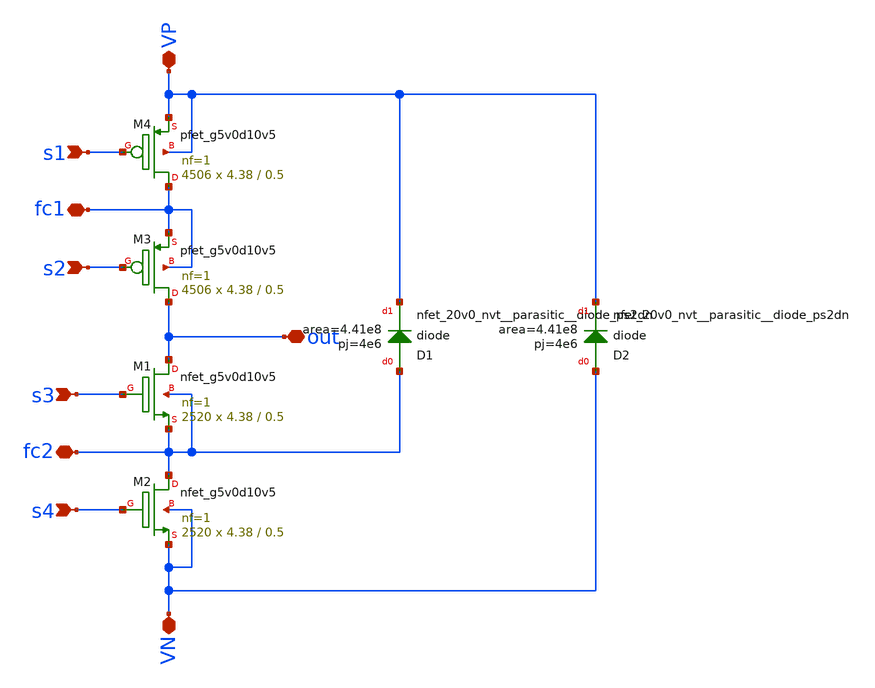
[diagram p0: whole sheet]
** sch_path: xschem/hierarchy_sch/power_stage_diode.sch
**.subckt power_stage_diode VP s1 s2 out s3 s4 VN fc1 fc2
*.iopin VP
*.ipin s1
*.ipin s2
*.iopin out
*.ipin s3
*.ipin s4
*.iopin VN
*.iopin fc1
*.iopin fc2
XM3 out s2 fc1 fc1 sky130_fd_pr__pfet_g5v0d10v5 L=0.5 W=4.38 nf=1 ad='int((nf+1)/2) * W/nf * 0.29' as='int((nf+2)/2) * W/nf * 0.29'
+ pd='2*int((nf+1)/2) * (W/nf + 0.29)' ps='2*int((nf+2)/2) * (W/nf + 0.29)' nrd='0.29 / W' nrs='0.29 / W'
+ sa=0 sb=0 sd=0 mult=4506 m=4506
XM4 fc1 s1 VP VP sky130_fd_pr__pfet_g5v0d10v5 L=0.5 W=4.38 nf=1 ad='int((nf+1)/2) * W/nf * 0.29' as='int((nf+2)/2) * W/nf * 0.29'
+ pd='2*int((nf+1)/2) * (W/nf + 0.29)' ps='2*int((nf+2)/2) * (W/nf + 0.29)' nrd='0.29 / W' nrs='0.29 / W'
+ sa=0 sb=0 sd=0 mult=4506 m=4506
XM1 out s3 fc2 fc2 sky130_fd_pr__nfet_g5v0d10v5 L=0.5 W=4.38 nf=1 ad='int((nf+1)/2) * W/nf * 0.29' as='int((nf+2)/2) * W/nf * 0.29'
+ pd='2*int((nf+1)/2) * (W/nf + 0.29)' ps='2*int((nf+2)/2) * (W/nf + 0.29)' nrd='0.29 / W' nrs='0.29 / W'
+ sa=0 sb=0 sd=0 mult=2520 m=2520
XM2 fc2 s4 VN VN sky130_fd_pr__nfet_g5v0d10v5 L=0.5 W=4.38 nf=1 ad='int((nf+1)/2) * W/nf * 0.29' as='int((nf+2)/2) * W/nf * 0.29'
+ pd='2*int((nf+1)/2) * (W/nf + 0.29)' ps='2*int((nf+2)/2) * (W/nf + 0.29)' nrd='0.29 / W' nrs='0.29 / W'
+ sa=0 sb=0 sd=0 mult=2520 m=2520
XD1 fc2 VP sky130_fd_pr__nfet_20v0_nvt__parasitic__diode_ps2dn area=4.41e8 pj=4e6
XD2 VN VP sky130_fd_pr__nfet_20v0_nvt__parasitic__diode_ps2dn area=4.41e8 pj=4e6
**.ends
.end
